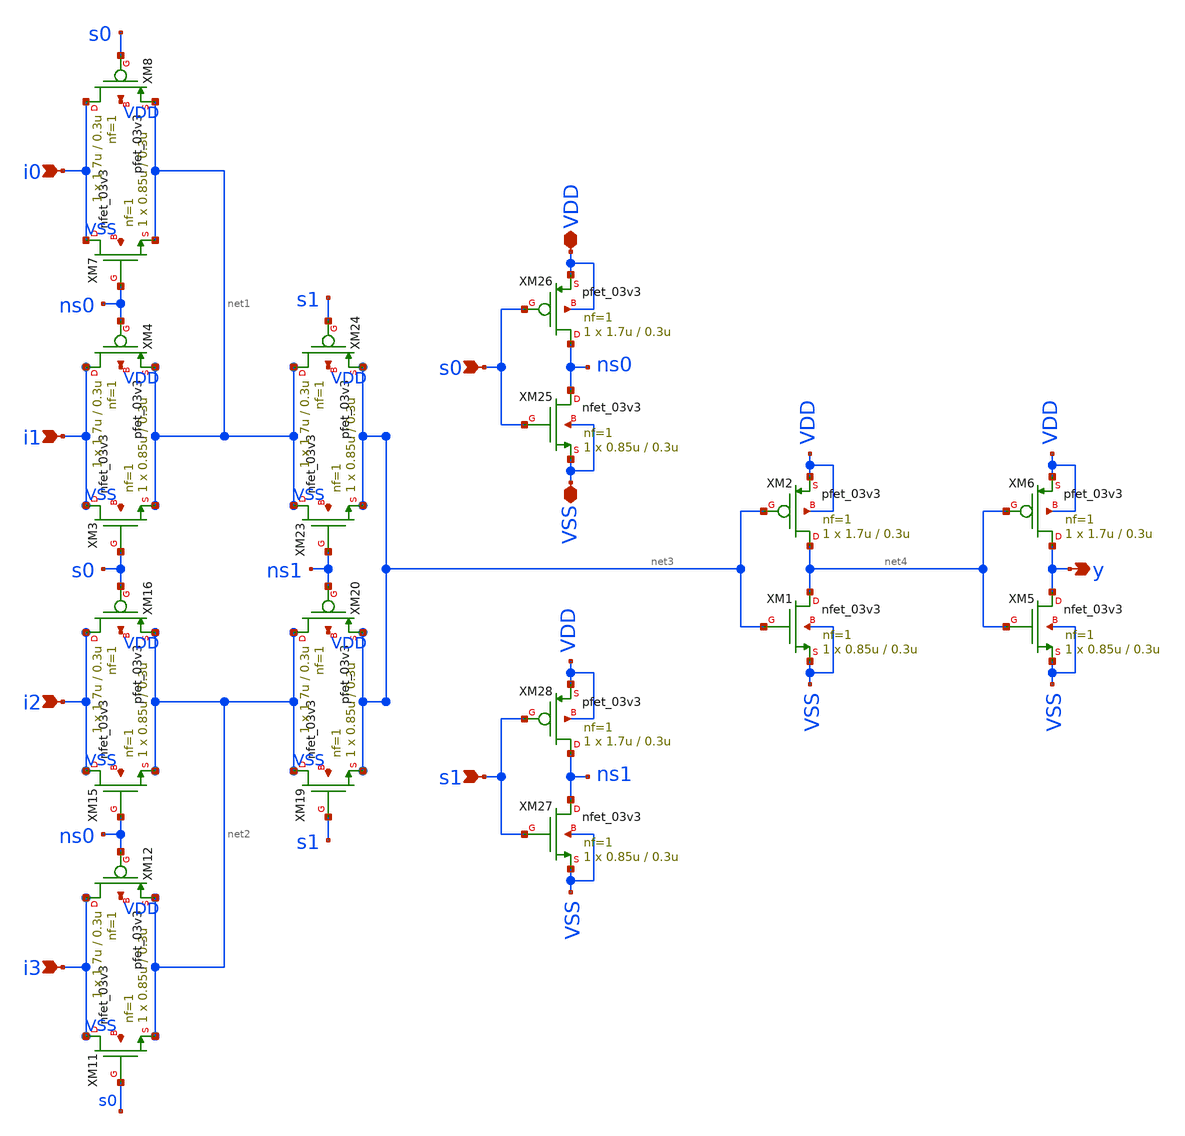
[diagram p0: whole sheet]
** sch_path: gf180mcu_osu_sc_gp9t3v3/xschem/gf180mcu_osu_sc_gp9t3v3__mux4_1.sch
**.subckt gf180mcu_osu_sc_gp9t3v3__mux4_1 i0 i1 i2 i3 y VDD VSS s0 s1
*.ipin i0
*.ipin i1
*.ipin i2
*.ipin i3
*.opin y
*.iopin VDD
*.iopin VSS
*.ipin s0
*.ipin s1
XM3 i1 s0 net1 VSS nfet_03v3 L=0.3u W=0.85u nf=1 ad='int((nf+1)/2) * W/nf * 0.18u' as='int((nf+2)/2) * W/nf * 0.18u'
+ pd='2*int((nf+1)/2) * (W/nf + 0.18u)' ps='2*int((nf+2)/2) * (W/nf + 0.18u)' nrd='0.18u / W' nrs='0.18u / W'
+ sa=0 sb=0 sd=0 m=1
XM4 i1 ns0 net1 VDD pfet_03v3 L=0.3u W=1.7u nf=1 ad='int((nf+1)/2) * W/nf * 0.18u' as='int((nf+2)/2) * W/nf * 0.18u'
+ pd='2*int((nf+1)/2) * (W/nf + 0.18u)' ps='2*int((nf+2)/2) * (W/nf + 0.18u)' nrd='0.18u / W' nrs='0.18u / W'
+ sa=0 sb=0 sd=0 m=1
XM7 i0 ns0 net1 VSS nfet_03v3 L=0.3u W=0.85u nf=1 ad='int((nf+1)/2) * W/nf * 0.18u' as='int((nf+2)/2) * W/nf * 0.18u'
+ pd='2*int((nf+1)/2) * (W/nf + 0.18u)' ps='2*int((nf+2)/2) * (W/nf + 0.18u)' nrd='0.18u / W' nrs='0.18u / W'
+ sa=0 sb=0 sd=0 m=1
XM8 i0 s0 net1 VDD pfet_03v3 L=0.3u W=1.7u nf=1 ad='int((nf+1)/2) * W/nf * 0.18u' as='int((nf+2)/2) * W/nf * 0.18u'
+ pd='2*int((nf+1)/2) * (W/nf + 0.18u)' ps='2*int((nf+2)/2) * (W/nf + 0.18u)' nrd='0.18u / W' nrs='0.18u / W'
+ sa=0 sb=0 sd=0 m=1
XM11 i3 s0 net2 VSS nfet_03v3 L=0.3u W=0.85u nf=1 ad='int((nf+1)/2) * W/nf * 0.18u' as='int((nf+2)/2) * W/nf * 0.18u'
+ pd='2*int((nf+1)/2) * (W/nf + 0.18u)' ps='2*int((nf+2)/2) * (W/nf + 0.18u)' nrd='0.18u / W' nrs='0.18u / W'
+ sa=0 sb=0 sd=0 m=1
XM12 i3 ns0 net2 VDD pfet_03v3 L=0.3u W=1.7u nf=1 ad='int((nf+1)/2) * W/nf * 0.18u' as='int((nf+2)/2) * W/nf * 0.18u'
+ pd='2*int((nf+1)/2) * (W/nf + 0.18u)' ps='2*int((nf+2)/2) * (W/nf + 0.18u)' nrd='0.18u / W' nrs='0.18u / W'
+ sa=0 sb=0 sd=0 m=1
XM15 i2 ns0 net2 VSS nfet_03v3 L=0.3u W=0.85u nf=1 ad='int((nf+1)/2) * W/nf * 0.18u' as='int((nf+2)/2) * W/nf * 0.18u'
+ pd='2*int((nf+1)/2) * (W/nf + 0.18u)' ps='2*int((nf+2)/2) * (W/nf + 0.18u)' nrd='0.18u / W' nrs='0.18u / W'
+ sa=0 sb=0 sd=0 m=1
XM16 i2 s0 net2 VDD pfet_03v3 L=0.3u W=1.7u nf=1 ad='int((nf+1)/2) * W/nf * 0.18u' as='int((nf+2)/2) * W/nf * 0.18u'
+ pd='2*int((nf+1)/2) * (W/nf + 0.18u)' ps='2*int((nf+2)/2) * (W/nf + 0.18u)' nrd='0.18u / W' nrs='0.18u / W'
+ sa=0 sb=0 sd=0 m=1
XM19 net2 s1 net3 VSS nfet_03v3 L=0.3u W=0.85u nf=1 ad='int((nf+1)/2) * W/nf * 0.18u' as='int((nf+2)/2) * W/nf * 0.18u'
+ pd='2*int((nf+1)/2) * (W/nf + 0.18u)' ps='2*int((nf+2)/2) * (W/nf + 0.18u)' nrd='0.18u / W' nrs='0.18u / W'
+ sa=0 sb=0 sd=0 m=1
XM20 net2 ns1 net3 VDD pfet_03v3 L=0.3u W=1.7u nf=1 ad='int((nf+1)/2) * W/nf * 0.18u' as='int((nf+2)/2) * W/nf * 0.18u'
+ pd='2*int((nf+1)/2) * (W/nf + 0.18u)' ps='2*int((nf+2)/2) * (W/nf + 0.18u)' nrd='0.18u / W' nrs='0.18u / W'
+ sa=0 sb=0 sd=0 m=1
XM23 net1 ns1 net3 VSS nfet_03v3 L=0.3u W=0.85u nf=1 ad='int((nf+1)/2) * W/nf * 0.18u' as='int((nf+2)/2) * W/nf * 0.18u'
+ pd='2*int((nf+1)/2) * (W/nf + 0.18u)' ps='2*int((nf+2)/2) * (W/nf + 0.18u)' nrd='0.18u / W' nrs='0.18u / W'
+ sa=0 sb=0 sd=0 m=1
XM24 net1 s1 net3 VDD pfet_03v3 L=0.3u W=1.7u nf=1 ad='int((nf+1)/2) * W/nf * 0.18u' as='int((nf+2)/2) * W/nf * 0.18u'
+ pd='2*int((nf+1)/2) * (W/nf + 0.18u)' ps='2*int((nf+2)/2) * (W/nf + 0.18u)' nrd='0.18u / W' nrs='0.18u / W'
+ sa=0 sb=0 sd=0 m=1
XM25 ns0 s0 VSS VSS nfet_03v3 L=0.3u W=0.85u nf=1 ad='int((nf+1)/2) * W/nf * 0.18u' as='int((nf+2)/2) * W/nf * 0.18u'
+ pd='2*int((nf+1)/2) * (W/nf + 0.18u)' ps='2*int((nf+2)/2) * (W/nf + 0.18u)' nrd='0.18u / W' nrs='0.18u / W'
+ sa=0 sb=0 sd=0 m=1
XM26 ns0 s0 VDD VDD pfet_03v3 L=0.3u W=1.7u nf=1 ad='int((nf+1)/2) * W/nf * 0.18u' as='int((nf+2)/2) * W/nf * 0.18u'
+ pd='2*int((nf+1)/2) * (W/nf + 0.18u)' ps='2*int((nf+2)/2) * (W/nf + 0.18u)' nrd='0.18u / W' nrs='0.18u / W'
+ sa=0 sb=0 sd=0 m=1
XM27 ns1 s1 VSS VSS nfet_03v3 L=0.3u W=0.85u nf=1 ad='int((nf+1)/2) * W/nf * 0.18u' as='int((nf+2)/2) * W/nf * 0.18u'
+ pd='2*int((nf+1)/2) * (W/nf + 0.18u)' ps='2*int((nf+2)/2) * (W/nf + 0.18u)' nrd='0.18u / W' nrs='0.18u / W'
+ sa=0 sb=0 sd=0 m=1
XM28 ns1 s1 VDD VDD pfet_03v3 L=0.3u W=1.7u nf=1 ad='int((nf+1)/2) * W/nf * 0.18u' as='int((nf+2)/2) * W/nf * 0.18u'
+ pd='2*int((nf+1)/2) * (W/nf + 0.18u)' ps='2*int((nf+2)/2) * (W/nf + 0.18u)' nrd='0.18u / W' nrs='0.18u / W'
+ sa=0 sb=0 sd=0 m=1
XM1 net4 net3 VSS VSS nfet_03v3 L=0.3u W=0.85u nf=1 ad='int((nf+1)/2) * W/nf * 0.18u' as='int((nf+2)/2) * W/nf * 0.18u'
+ pd='2*int((nf+1)/2) * (W/nf + 0.18u)' ps='2*int((nf+2)/2) * (W/nf + 0.18u)' nrd='0.18u / W' nrs='0.18u / W'
+ sa=0 sb=0 sd=0 m=1
XM2 net4 net3 VDD VDD pfet_03v3 L=0.3u W=1.7u nf=1 ad='int((nf+1)/2) * W/nf * 0.18u' as='int((nf+2)/2) * W/nf * 0.18u'
+ pd='2*int((nf+1)/2) * (W/nf + 0.18u)' ps='2*int((nf+2)/2) * (W/nf + 0.18u)' nrd='0.18u / W' nrs='0.18u / W'
+ sa=0 sb=0 sd=0 m=1
XM5 y net4 VSS VSS nfet_03v3 L=0.3u W=0.85u nf=1 ad='int((nf+1)/2) * W/nf * 0.18u' as='int((nf+2)/2) * W/nf * 0.18u'
+ pd='2*int((nf+1)/2) * (W/nf + 0.18u)' ps='2*int((nf+2)/2) * (W/nf + 0.18u)' nrd='0.18u / W' nrs='0.18u / W'
+ sa=0 sb=0 sd=0 m=1
XM6 y net4 VDD VDD pfet_03v3 L=0.3u W=1.7u nf=1 ad='int((nf+1)/2) * W/nf * 0.18u' as='int((nf+2)/2) * W/nf * 0.18u'
+ pd='2*int((nf+1)/2) * (W/nf + 0.18u)' ps='2*int((nf+2)/2) * (W/nf + 0.18u)' nrd='0.18u / W' nrs='0.18u / W'
+ sa=0 sb=0 sd=0 m=1
**.ends
.end
